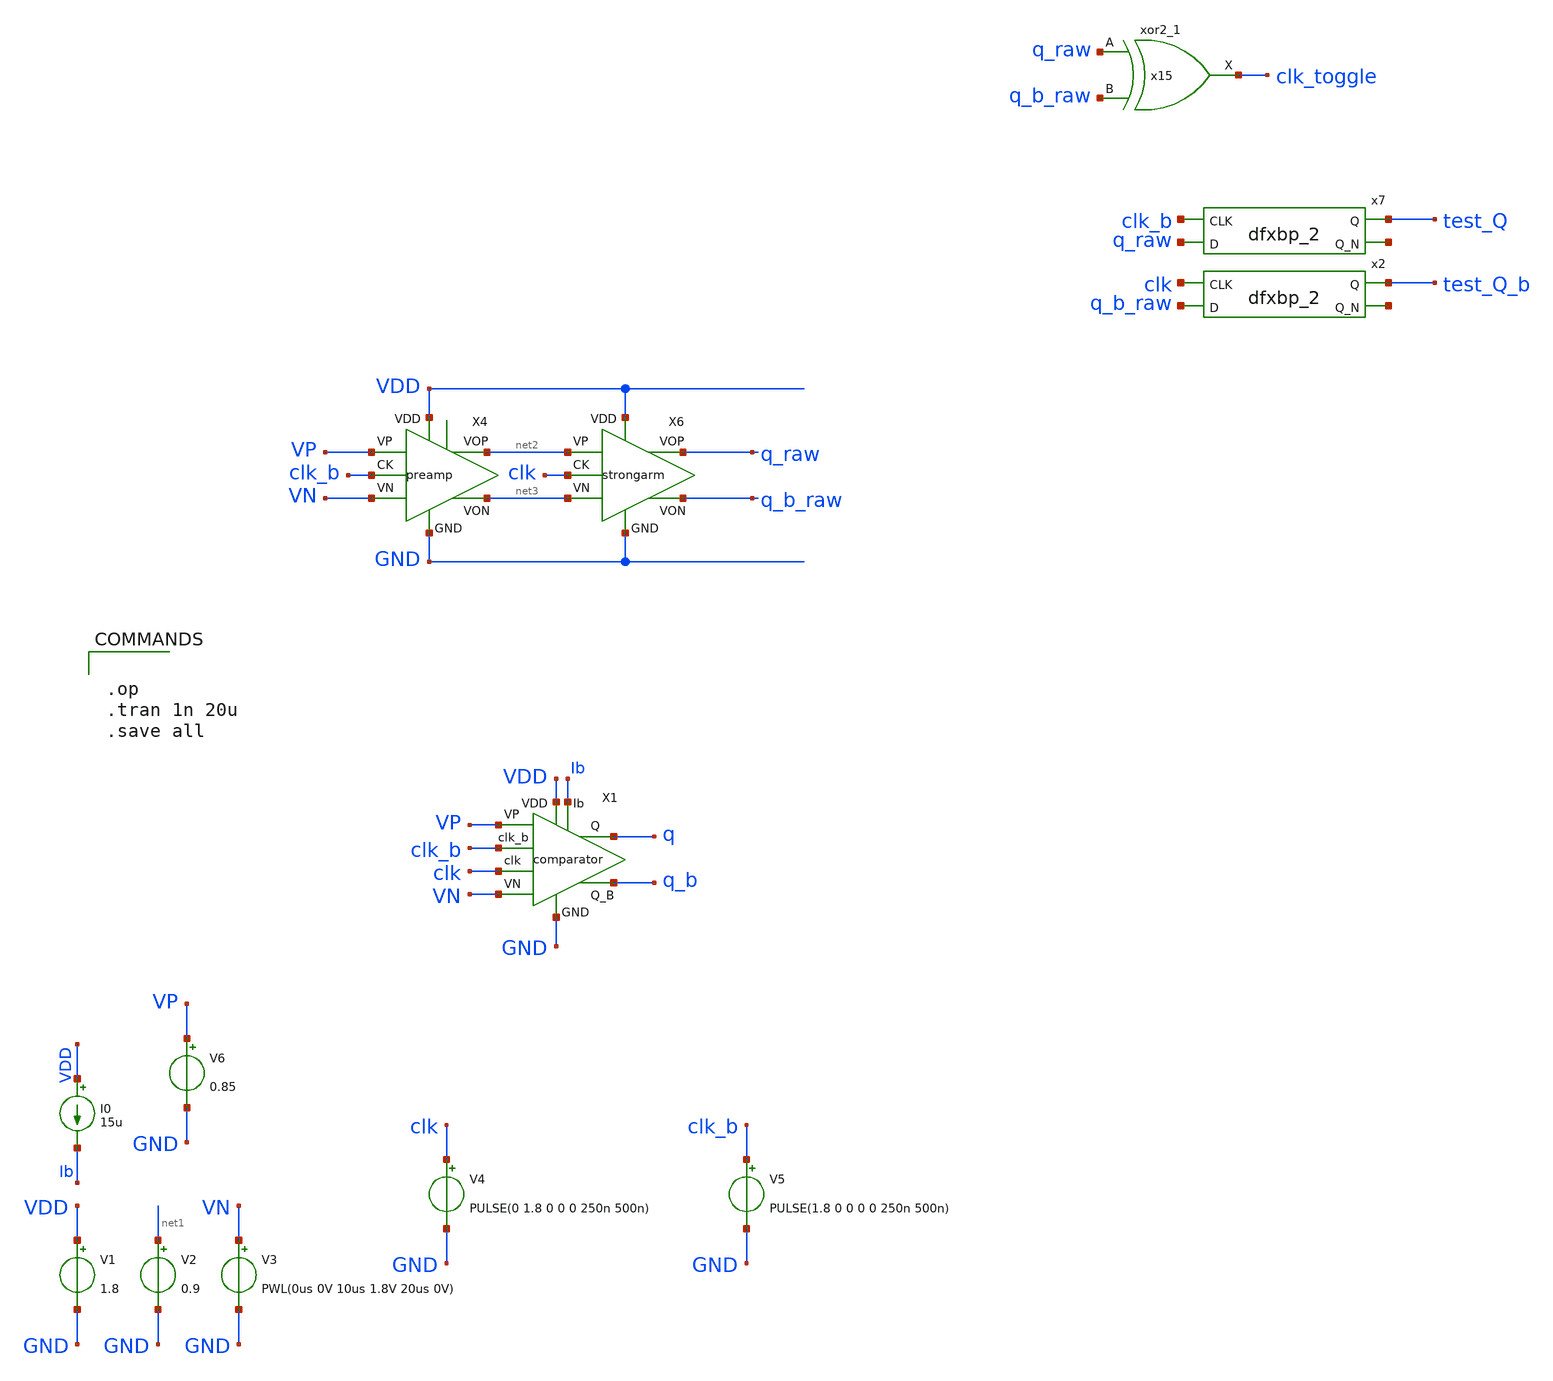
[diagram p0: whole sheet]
** sch_path: xschem/comparator/comparator_tb.sch
.lib $::SKYWATER_MODELS/sky130.lib.spice tt
.include $::SKYWATER_STDCELLS/sky130_fd_sc_hd.spice

**.subckt comparator_tb
V1 VDD GND 1.8
V2 net1 GND 0.9
V3 VN GND PWL(0us 0V 10us 1.8V 20us 0V)
V4 clk GND PULSE(0 1.8 0 0 0 250n 500n)
I0 VDD Ib 15u
V5 clk_b GND PULSE(1.8 0 0 0 0 250n 500n)
X1 VP VN GND q_b q VDD clk Ib clk_b comparator
V6 VP GND 0.85
X4 VP VN GND net3 net2 VDD clk_b preamp
X6 net2 net3 GND q_b_raw q_raw VDD clk strongarm
x7 clk_b q_raw GND GND VDD VDD test_Q net4 sky130_fd_sc_hd__dfxbp_2
x15 q_raw q_b_raw VGND VGND VDD VDD clk_toggle sky130_fd_sc_hd__xor2_1
x2 clk q_b_raw GND GND VDD VDD test_Q_b net5 sky130_fd_sc_hd__dfxbp_2
**** begin user architecture code


.op
.tran 1n 20u
.save all


**** end user architecture code
**.ends
.end
